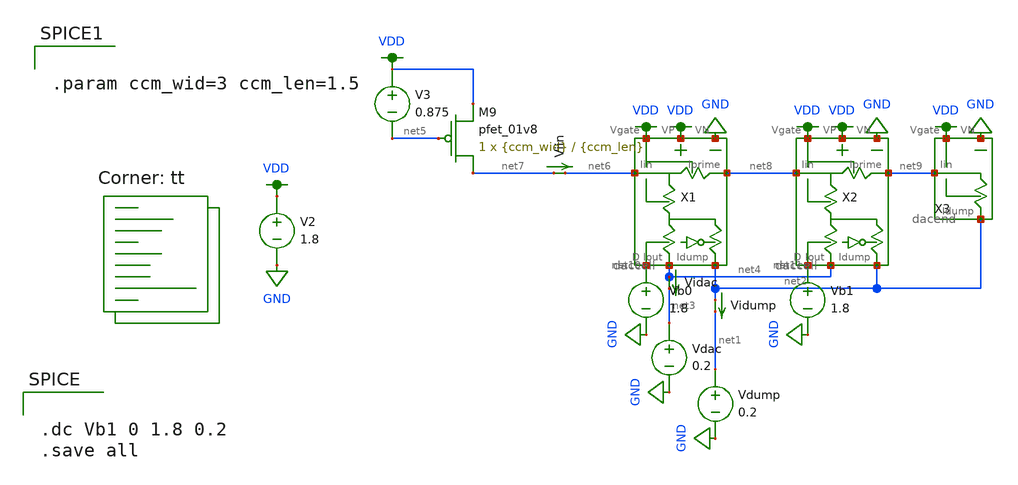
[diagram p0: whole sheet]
** sch_path: test_daccell.sch
**.subckt test_daccell
X1 net10 net2 VDD GND net4 net6 net8 VDD daccell
V2 VDD GND 1.8
Vb0 net10 GND 1.8
Vdac net3 GND 0.2
Vdump net1 GND 0.2
Vidac net4 net3 0
.save i(vidac)
Vidump net2 net1 0
.save i(vidump)
V3 VDD net5 0.875
XM9 net7 net5 VDD VP sky130_fd_pr__pfet_01v8 L={ccm_len} W={ccm_wid} nf=1 ad='int((nf+1)/2) * W/nf * 0.29'
+ as='int((nf+2)/2) * W/nf * 0.29' pd='2*int((nf+1)/2) * (W/nf + 0.29)' ps='2*int((nf+2)/2) * (W/nf + 0.29)'
+ nrd='0.29 / W' nrs='0.29 / W' sa=0 sb=0 sd=0 mult=1 m=1
Viin net7 net6 0
.save i(viin)
X2 net11 net2 VDD GND net4 net8 net9 VDD daccell
Vb1 net11 GND 1.8
X3 net2 GND net9 VDD dacend
**** begin user architecture code
.lib $::SKYWATER_MODELS/sky130.lib.spice tt


.dc Vb1 0 1.8 0.2
.save all



.param ccm_wid=3 ccm_len=1.5


**** end user architecture code
**.ends
.GLOBAL GND
.GLOBAL VDD
.end
